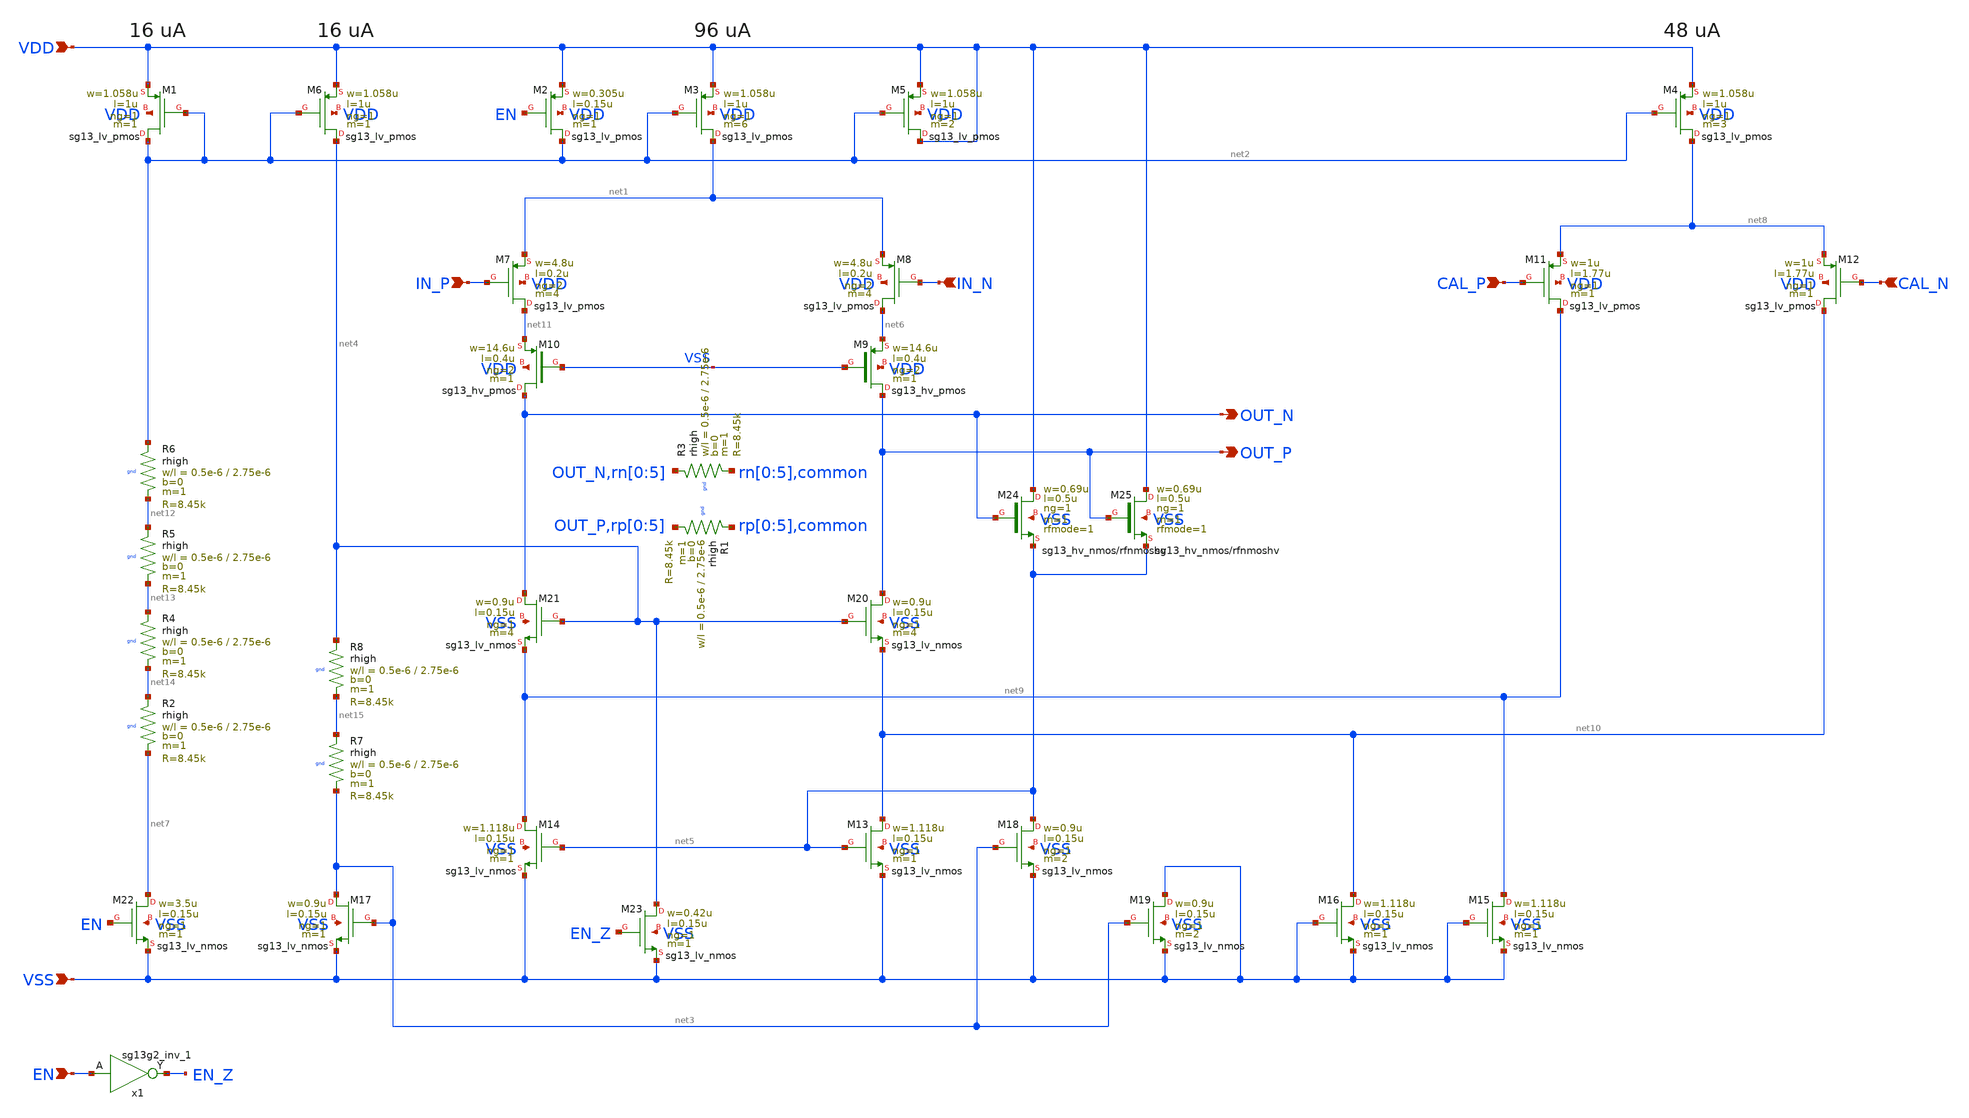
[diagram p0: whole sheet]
** sch_path: schematic/preamplifier/preamplifier.sch
**.subckt preamplifier VDD VSS IN_P IN_N OUT_P OUT_N EN CAL_P CAL_N
*.ipin VDD
*.ipin VSS
*.ipin IN_P
*.ipin IN_N
*.opin OUT_P
*.opin OUT_N
*.ipin EN
*.ipin CAL_P
*.ipin CAL_N
XM3 net1 net2 VDD VDD sg13_lv_pmos w=1.058u l=1u ng=1 m=6 mm_ok=1
XM2 net2 EN VDD VDD sg13_lv_pmos w=0.305u l=0.15u ng=1 m=1 mm_ok=1
XM5 VDD net2 VDD VDD sg13_lv_pmos w=1.058u l=1u ng=1 m=2 mm_ok=1
XM6 net4 net2 VDD VDD sg13_lv_pmos w=1.058u l=1u ng=1 m=1 mm_ok=1
XM1 net2 net2 VDD VDD sg13_lv_pmos w=1.058u l=1u ng=1 m=1 mm_ok=1
XM4 net8 net2 VDD VDD sg13_lv_pmos w=1.058u l=1u ng=1 m=3 mm_ok=1
XM7 net11 IN_P net1 VDD sg13_lv_pmos w=4.8u l=0.2u ng=2 m=4 mm_ok=1
XM8 net6 IN_N net1 VDD sg13_lv_pmos w=4.8u l=0.2u ng=2 m=4 mm_ok=1
XM9 OUT_P VSS net6 VDD sg13_hv_pmos w=14.6u l=0.4u ng=2 m=1 mm_ok=1
XM10 OUT_N VSS net11 VDD sg13_hv_pmos w=14.6u l=0.4u ng=2 m=1 mm_ok=1
XM11 net9 CAL_P net8 VDD sg13_lv_pmos w=1u l=1.77u ng=1 m=1 mm_ok=1
XM12 net10 CAL_N net8 VDD sg13_lv_pmos w=1u l=1.77u ng=1 m=1 mm_ok=1
XM13 net10 net5 VSS VSS sg13_lv_nmos w=1.118u l=0.15u ng=1 m=1 mm_ok=1
XM14 net9 net5 VSS VSS sg13_lv_nmos w=1.118u l=0.15u ng=1 m=1 mm_ok=1
XM15 net9 VSS VSS VSS sg13_lv_nmos w=1.118u l=0.15u ng=1 m=1 mm_ok=1
XM16 net10 VSS VSS VSS sg13_lv_nmos w=1.118u l=0.15u ng=1 m=1 mm_ok=1
XM17 net3 net3 VSS VSS sg13_lv_nmos w=0.9u l=0.15u ng=1 m=1 mm_ok=1
XM18 net5 net3 VSS VSS sg13_lv_nmos w=0.9u l=0.15u ng=1 m=2 mm_ok=1
XM19 VSS net3 VSS VSS sg13_lv_nmos w=0.9u l=0.15u ng=1 m=2 mm_ok=1
x1 EN_Z EN VDD VSS sg13g2_inv_1
XM20 OUT_P net4 net10 VSS sg13_lv_nmos w=0.9u l=0.15u ng=1 m=4 mm_ok=1
XM21 OUT_N net4 net9 VSS sg13_lv_nmos w=0.9u l=0.15u ng=1 m=4 mm_ok=1
XM22 net7 EN VSS VSS sg13_lv_nmos w=3.5u l=0.15u ng=1 m=1 mm_ok=1
XM23 net4 EN_Z VSS VSS sg13_lv_nmos w=0.42u l=0.15u ng=1 m=1 mm_ok=1
XM24 VDD OUT_N net5 VSS sg13_hv_nmos w=0.69u l=0.5u ng=1 m=1 rfmode=1 mm_ok=1
XM25 VDD OUT_P net5 VSS sg13_hv_nmos w=0.69u l=0.5u ng=1 m=1 rfmode=1 mm_ok=1
XR3 OUT_N rn[0] gnd rhigh w=0.5e-6 l=2.75e-6 m=1 b=0 mm_ok=1
XR1 rp[0] OUT_P gnd rhigh w=0.5e-6 l=2.75e-6 m=1 b=0 mm_ok=1
XR2 net14 net7 gnd rhigh w=0.5e-6 l=2.75e-6 m=1 b=0 mm_ok=1
XR4 net13 net14 gnd rhigh w=0.5e-6 l=2.75e-6 m=1 b=0 mm_ok=1
XR5 net12 net13 gnd rhigh w=0.5e-6 l=2.75e-6 m=1 b=0 mm_ok=1
XR6 net2 net12 gnd rhigh w=0.5e-6 l=2.75e-6 m=1 b=0 mm_ok=1
XR7 net15 net3 gnd rhigh w=0.5e-6 l=2.75e-6 m=1 b=0 mm_ok=1
XR8 net4 net15 gnd rhigh w=0.5e-6 l=2.75e-6 m=1 b=0 mm_ok=1
**.ends

* expanding   symbol:  sg13g2_stdcells/sg13g2_inv_1.sym # of pins=2
** sym_path: sg13g2_stdcells/sg13g2_inv_1.sym
** sch_path: sg13g2_stdcells/sg13g2_inv_1.sch
.subckt sg13g2_inv_1 Y A VDD VSS
*.opin Y
*.ipin A
*.iopin VDD
*.iopin VSS
XM1 Y A VSS VSS sg13_lv_nmos w=740.00n l=130.00n ng=1 m=1 mm_ok=1
XM2 Y A VDD VDD sg13_lv_pmos w=1.12u l=130.00n ng=1 m=1 mm_ok=1
.ends

.end
